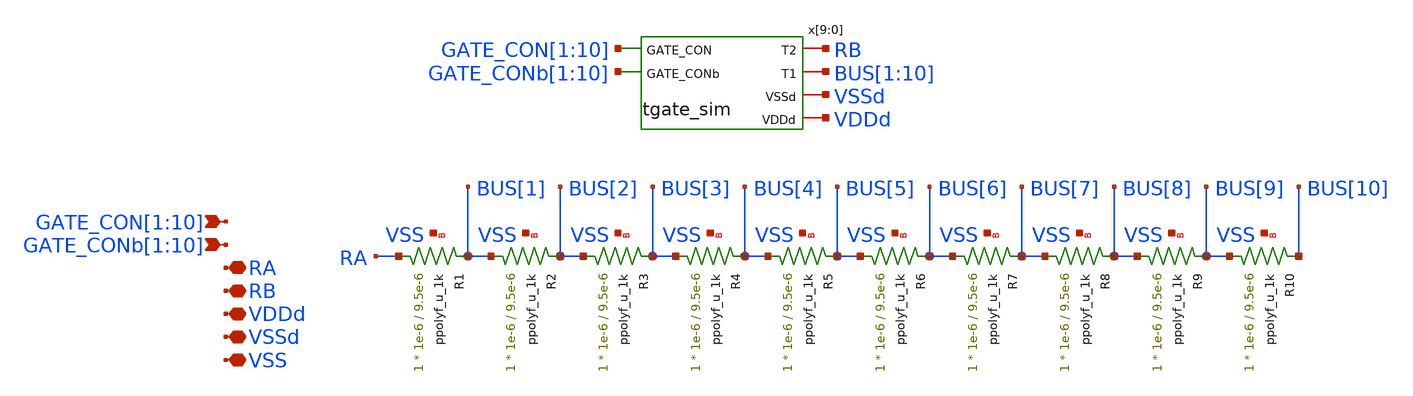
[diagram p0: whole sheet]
** sch_path: designs/libs/core_passive_array/sim_res_10x10k/sim_res_10x10k.sch
**.subckt sim_res_10x10k
*+ GATE_CON[1],GATE_CON[2],GATE_CON[3],GATE_CON[4],GATE_CON[5],GATE_CON[6],GATE_CON[7],GATE_CON[8],GATE_CON[9],GATE_CON[10]
*+ GATE_CONb[1],GATE_CONb[2],GATE_CONb[3],GATE_CONb[4],GATE_CONb[5],GATE_CONb[6],GATE_CONb[7],GATE_CONb[8],GATE_CONb[9],GATE_CONb[10] RA RB VDDd VSSd VSS
*.ipin
*+ GATE_CON[1],GATE_CON[2],GATE_CON[3],GATE_CON[4],GATE_CON[5],GATE_CON[6],GATE_CON[7],GATE_CON[8],GATE_CON[9],GATE_CON[10]
*.ipin
*+ GATE_CONb[1],GATE_CONb[2],GATE_CONb[3],GATE_CONb[4],GATE_CONb[5],GATE_CONb[6],GATE_CONb[7],GATE_CONb[8],GATE_CONb[9],GATE_CONb[10]
*.iopin RA
*.iopin RB
*.iopin VDDd
*.iopin VSSd
*.iopin VSS
XR1 RA BUS[1] VSS ppolyf_u_1k r_width=1e-6 r_length=9.5e-6 m=1
XR2 BUS[1] BUS[2] VSS ppolyf_u_1k r_width=1e-6 r_length=9.5e-6 m=1
XR3 BUS[2] BUS[3] VSS ppolyf_u_1k r_width=1e-6 r_length=9.5e-6 m=1
XR4 BUS[3] BUS[4] VSS ppolyf_u_1k r_width=1e-6 r_length=9.5e-6 m=1
XR5 BUS[4] BUS[5] VSS ppolyf_u_1k r_width=1e-6 r_length=9.5e-6 m=1
XR6 BUS[5] BUS[6] VSS ppolyf_u_1k r_width=1e-6 r_length=9.5e-6 m=1
XR7 BUS[6] BUS[7] VSS ppolyf_u_1k r_width=1e-6 r_length=9.5e-6 m=1
XR8 BUS[7] BUS[8] VSS ppolyf_u_1k r_width=1e-6 r_length=9.5e-6 m=1
XR9 BUS[8] BUS[9] VSS ppolyf_u_1k r_width=1e-6 r_length=9.5e-6 m=1
XR10 BUS[9] BUS[10] VSS ppolyf_u_1k r_width=1e-6 r_length=9.5e-6 m=1
x[9] RB GATE_CON[1] GATE_CONb[1] BUS[1] VSSd VDDd tgate_sim
x[8] RB GATE_CON[2] GATE_CONb[2] BUS[2] VSSd VDDd tgate_sim
x[7] RB GATE_CON[3] GATE_CONb[3] BUS[3] VSSd VDDd tgate_sim
x[6] RB GATE_CON[4] GATE_CONb[4] BUS[4] VSSd VDDd tgate_sim
x[5] RB GATE_CON[5] GATE_CONb[5] BUS[5] VSSd VDDd tgate_sim
x[4] RB GATE_CON[6] GATE_CONb[6] BUS[6] VSSd VDDd tgate_sim
x[3] RB GATE_CON[7] GATE_CONb[7] BUS[7] VSSd VDDd tgate_sim
x[2] RB GATE_CON[8] GATE_CONb[8] BUS[8] VSSd VDDd tgate_sim
x[1] RB GATE_CON[9] GATE_CONb[9] BUS[9] VSSd VDDd tgate_sim
x[0] RB GATE_CON[10] GATE_CONb[10] BUS[10] VSSd VDDd tgate_sim
**.ends
.end
